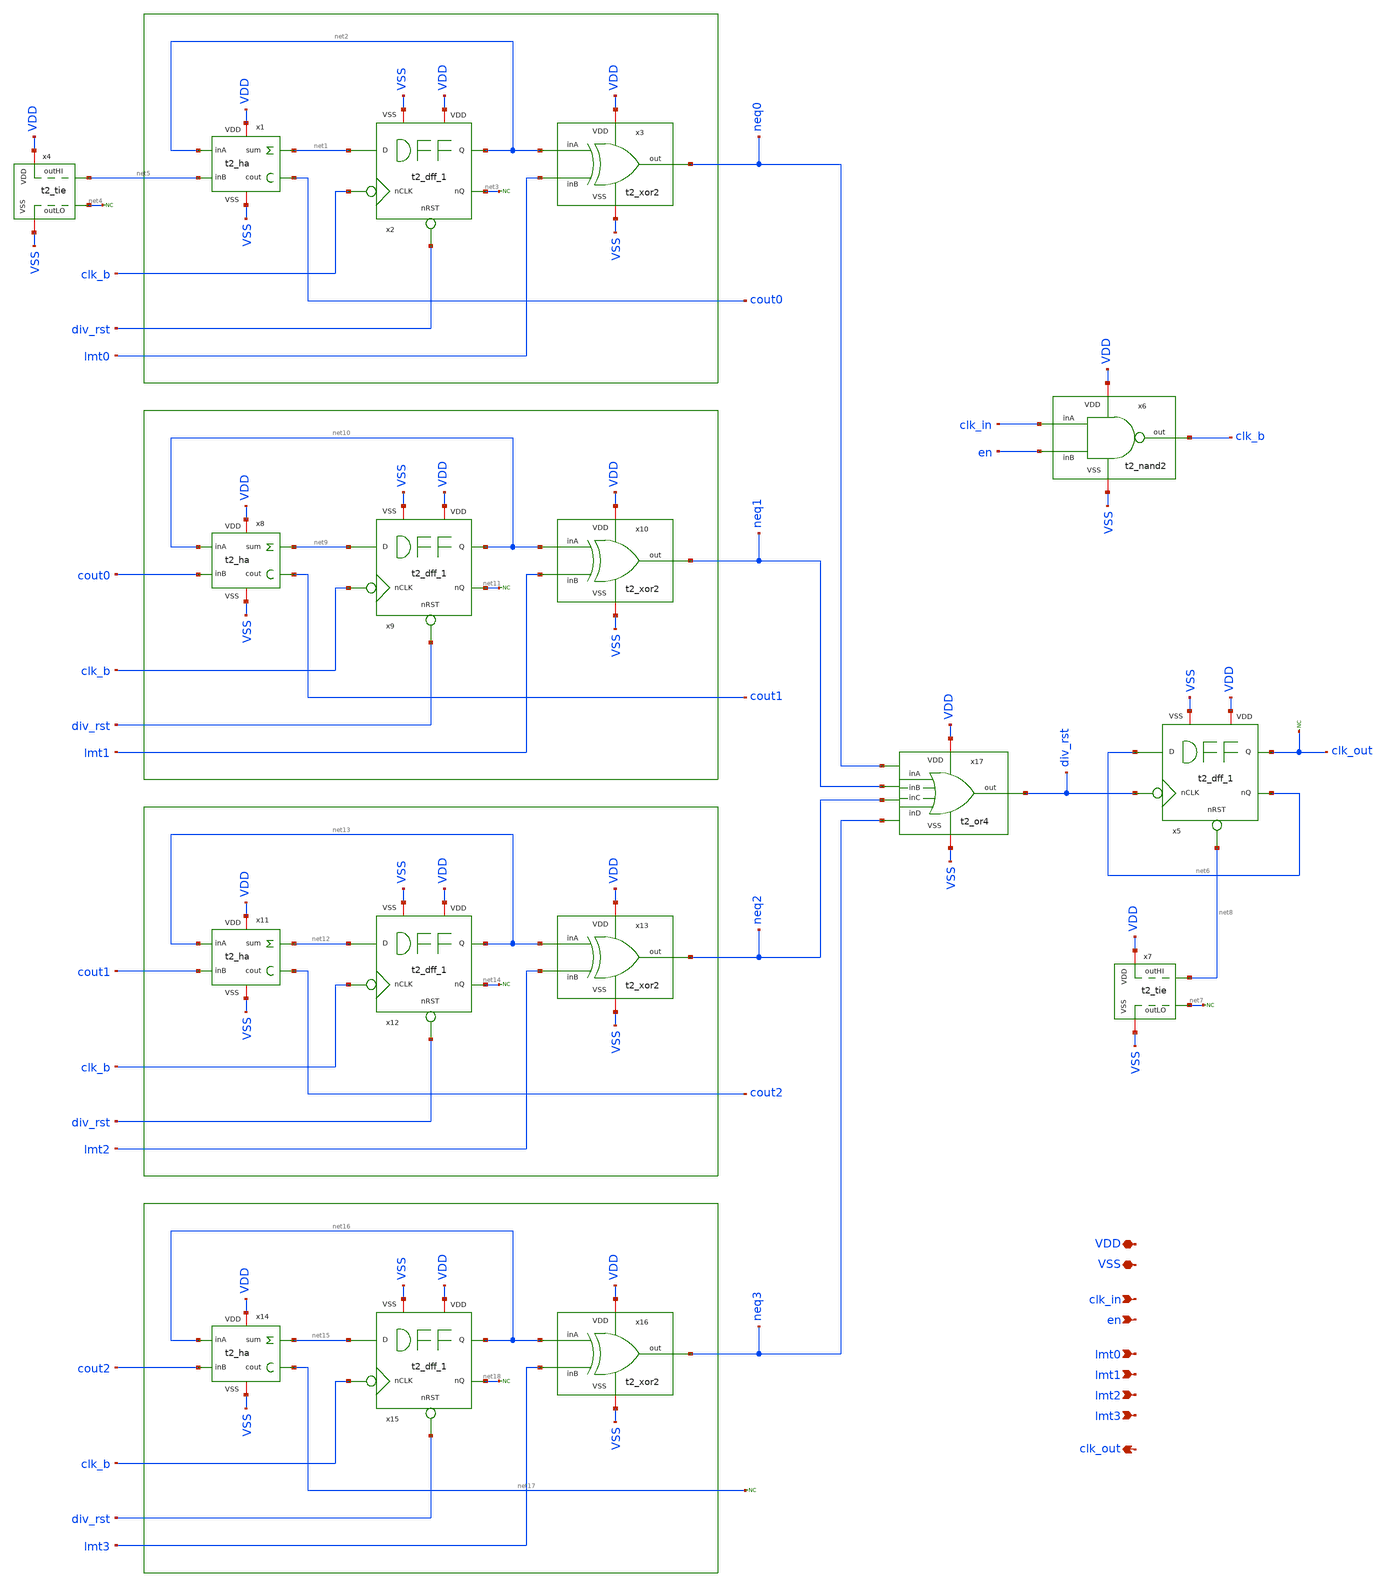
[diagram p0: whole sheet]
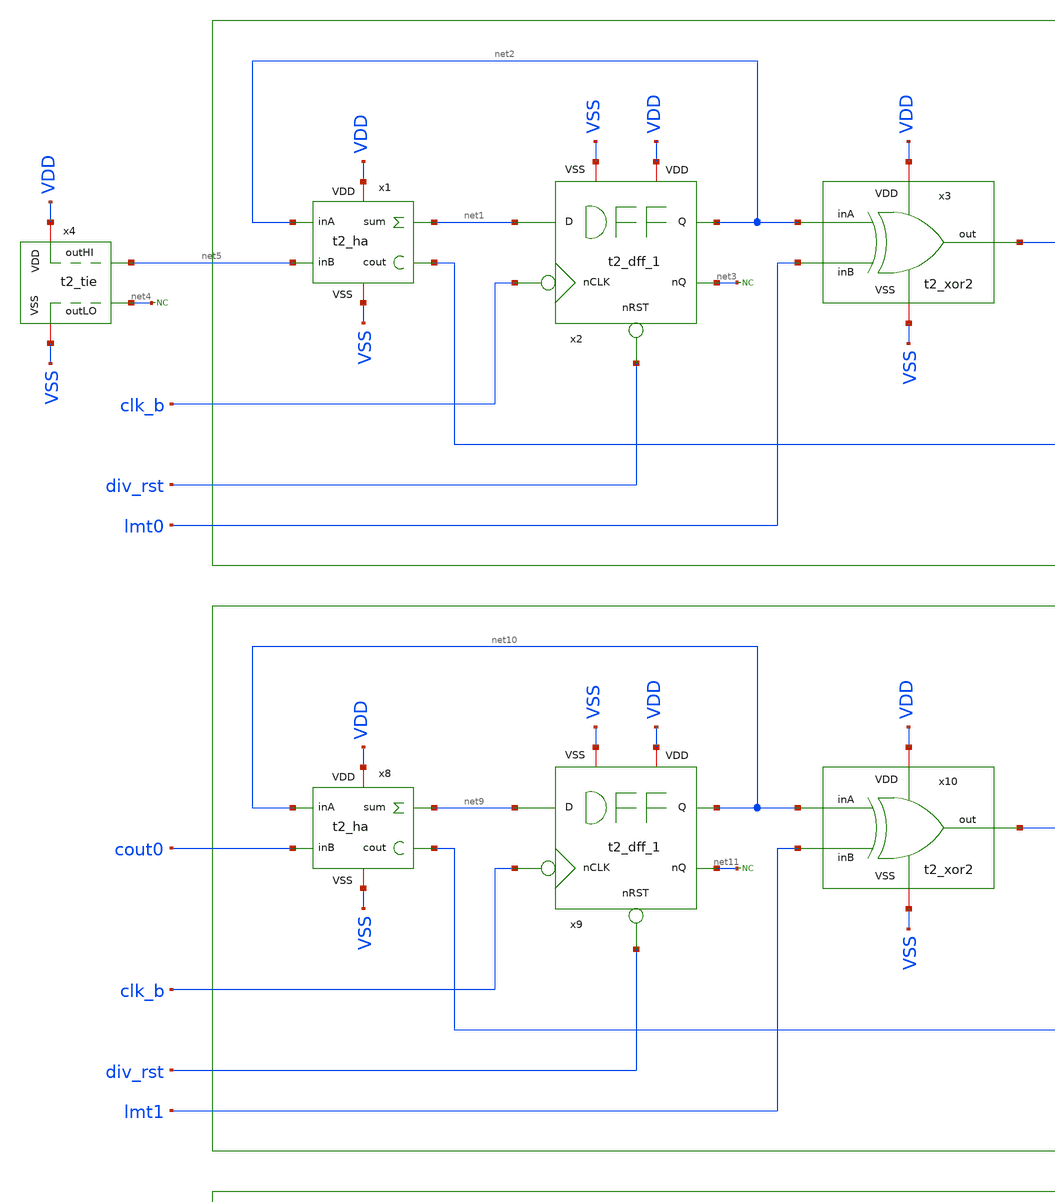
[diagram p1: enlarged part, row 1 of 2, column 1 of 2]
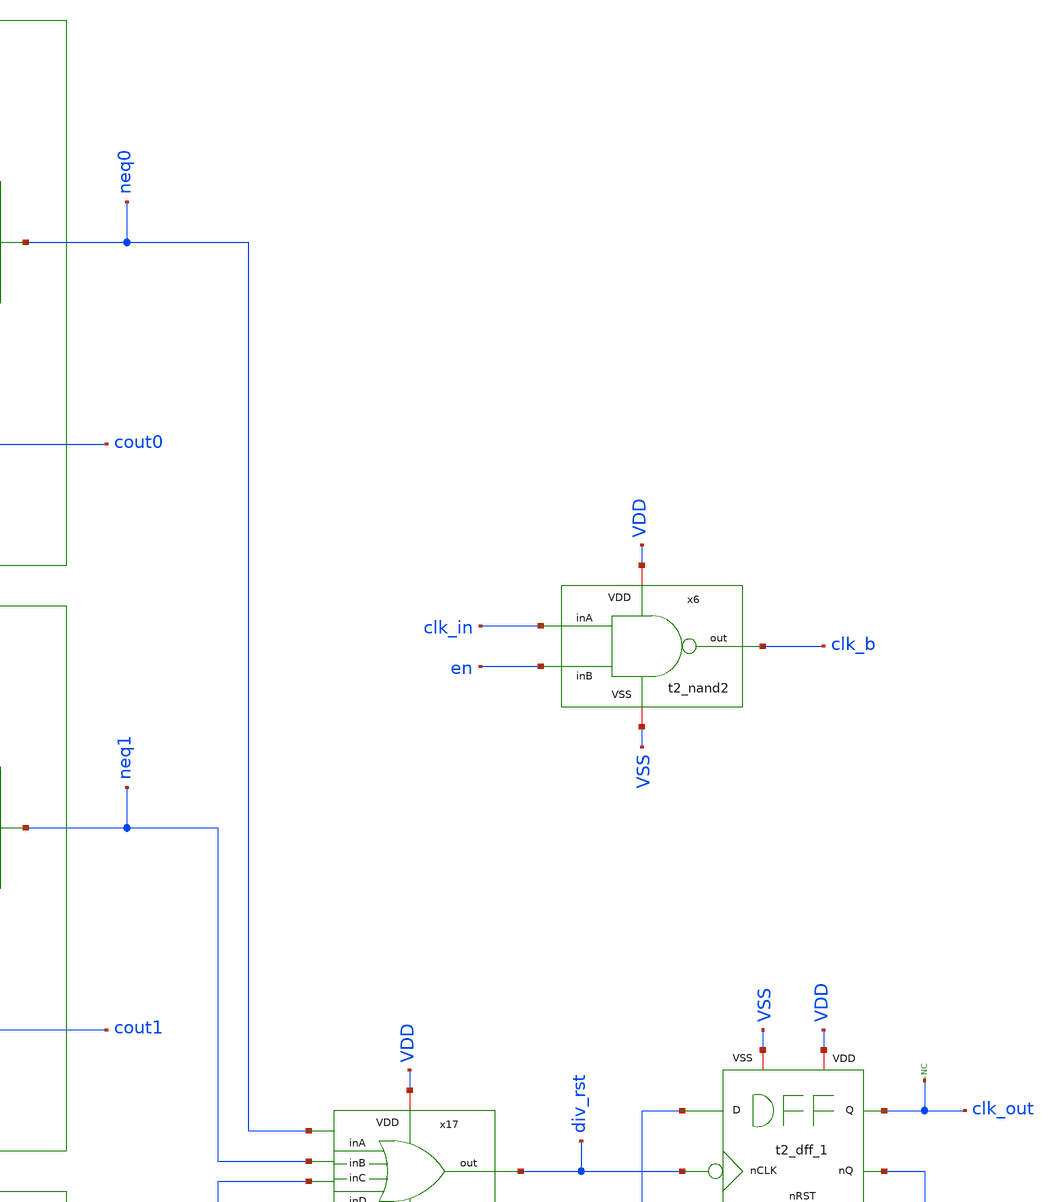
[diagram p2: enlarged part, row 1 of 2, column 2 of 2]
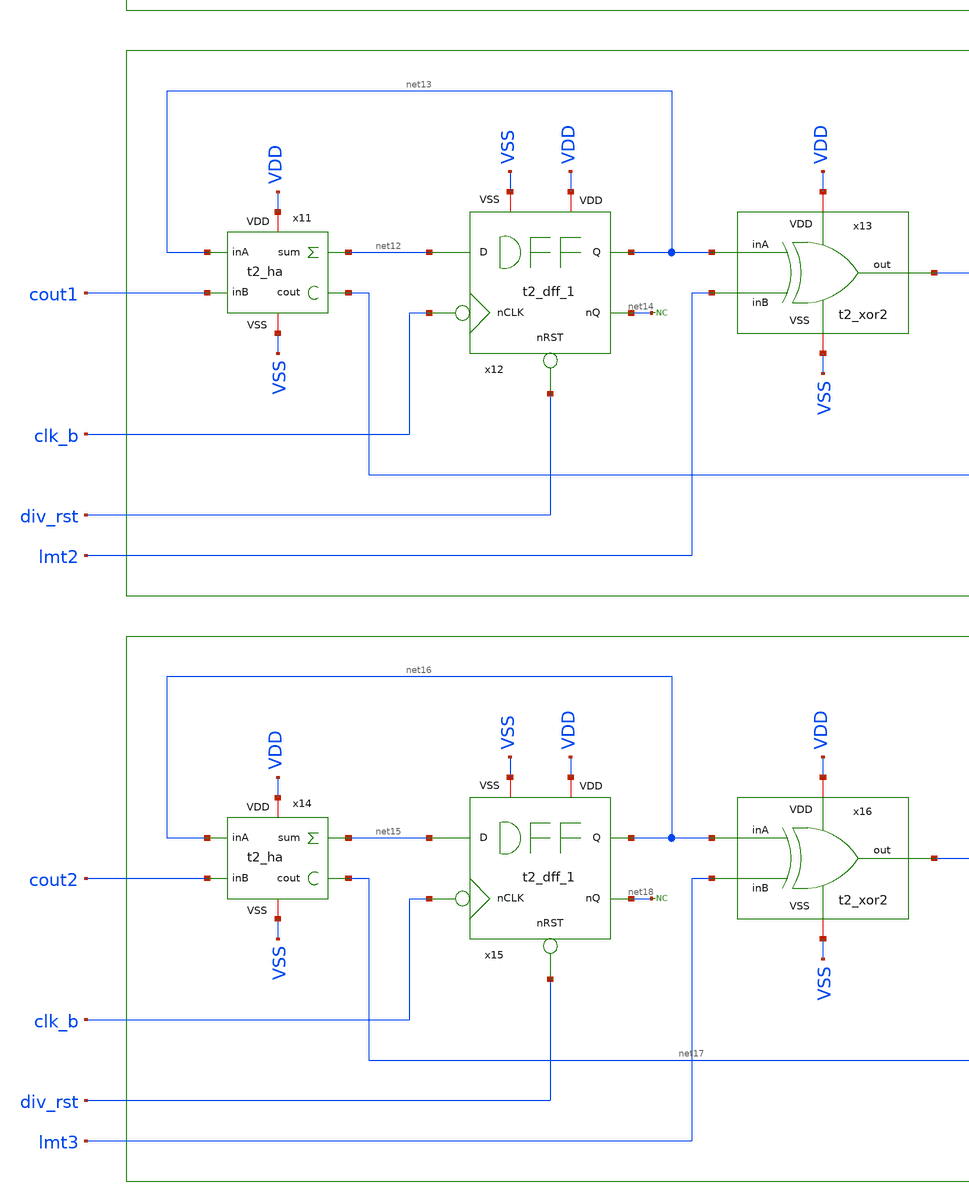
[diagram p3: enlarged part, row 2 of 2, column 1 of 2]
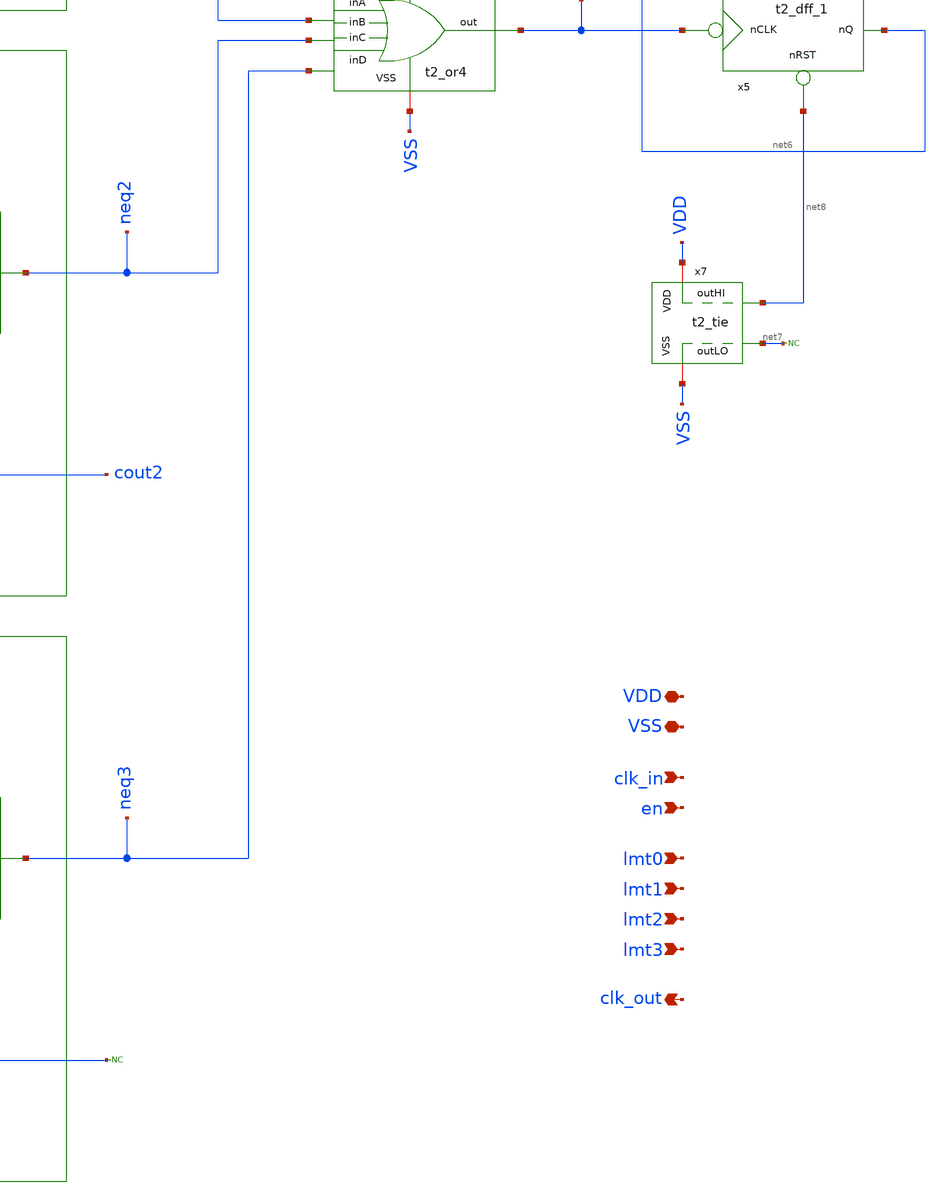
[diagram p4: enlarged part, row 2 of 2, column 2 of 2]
** sch_path: Team Designs/Team 2 Design/design_data/xschem/t2_freq_divider.sch
**.subckt t2_freq_divider VSS lmt0 VDD clk_out lmt1 lmt2 lmt3 clk_in en
*.iopin VSS
*.ipin lmt0
*.iopin VDD
*.opin clk_out
*.ipin lmt1
*.ipin lmt2
*.ipin lmt3
*.ipin clk_in
*.ipin en
x1 VDD VSS net2 net5 net1 cout0 t2_ha
x2 VDD VSS net1 clk_b div_rst net2 net3 t2_dff_1
x3 VDD VSS net2 lmt0 neq0 t2_xor2
* noconn #net3
x4 VDD VSS net5 net4 t2_tie
* noconn #net4
* noconn clk_out
x5 VDD VSS net6 div_rst net8 clk_out net6 t2_dff_1
x7 VDD VSS net8 net7 t2_tie
* noconn #net7
x8 VDD VSS net10 cout0 net9 cout1 t2_ha
x9 VDD VSS net9 clk_b div_rst net10 net11 t2_dff_1
x10 VDD VSS net10 lmt1 neq1 t2_xor2
* noconn #net11
x11 VDD VSS net13 cout1 net12 cout2 t2_ha
x12 VDD VSS net12 clk_b div_rst net13 net14 t2_dff_1
x13 VDD VSS net13 lmt2 neq2 t2_xor2
* noconn #net14
x14 VDD VSS net16 cout2 net15 net17 t2_ha
x15 VDD VSS net15 clk_b div_rst net16 net18 t2_dff_1
x16 VDD VSS net16 lmt3 neq3 t2_xor2
* noconn #net18
* noconn #net17
x17 VDD VSS neq0 neq1 neq2 neq3 div_rst t2_or4
x6 VDD clk_in en clk_b VSS t2_nand2
**.ends
.end
